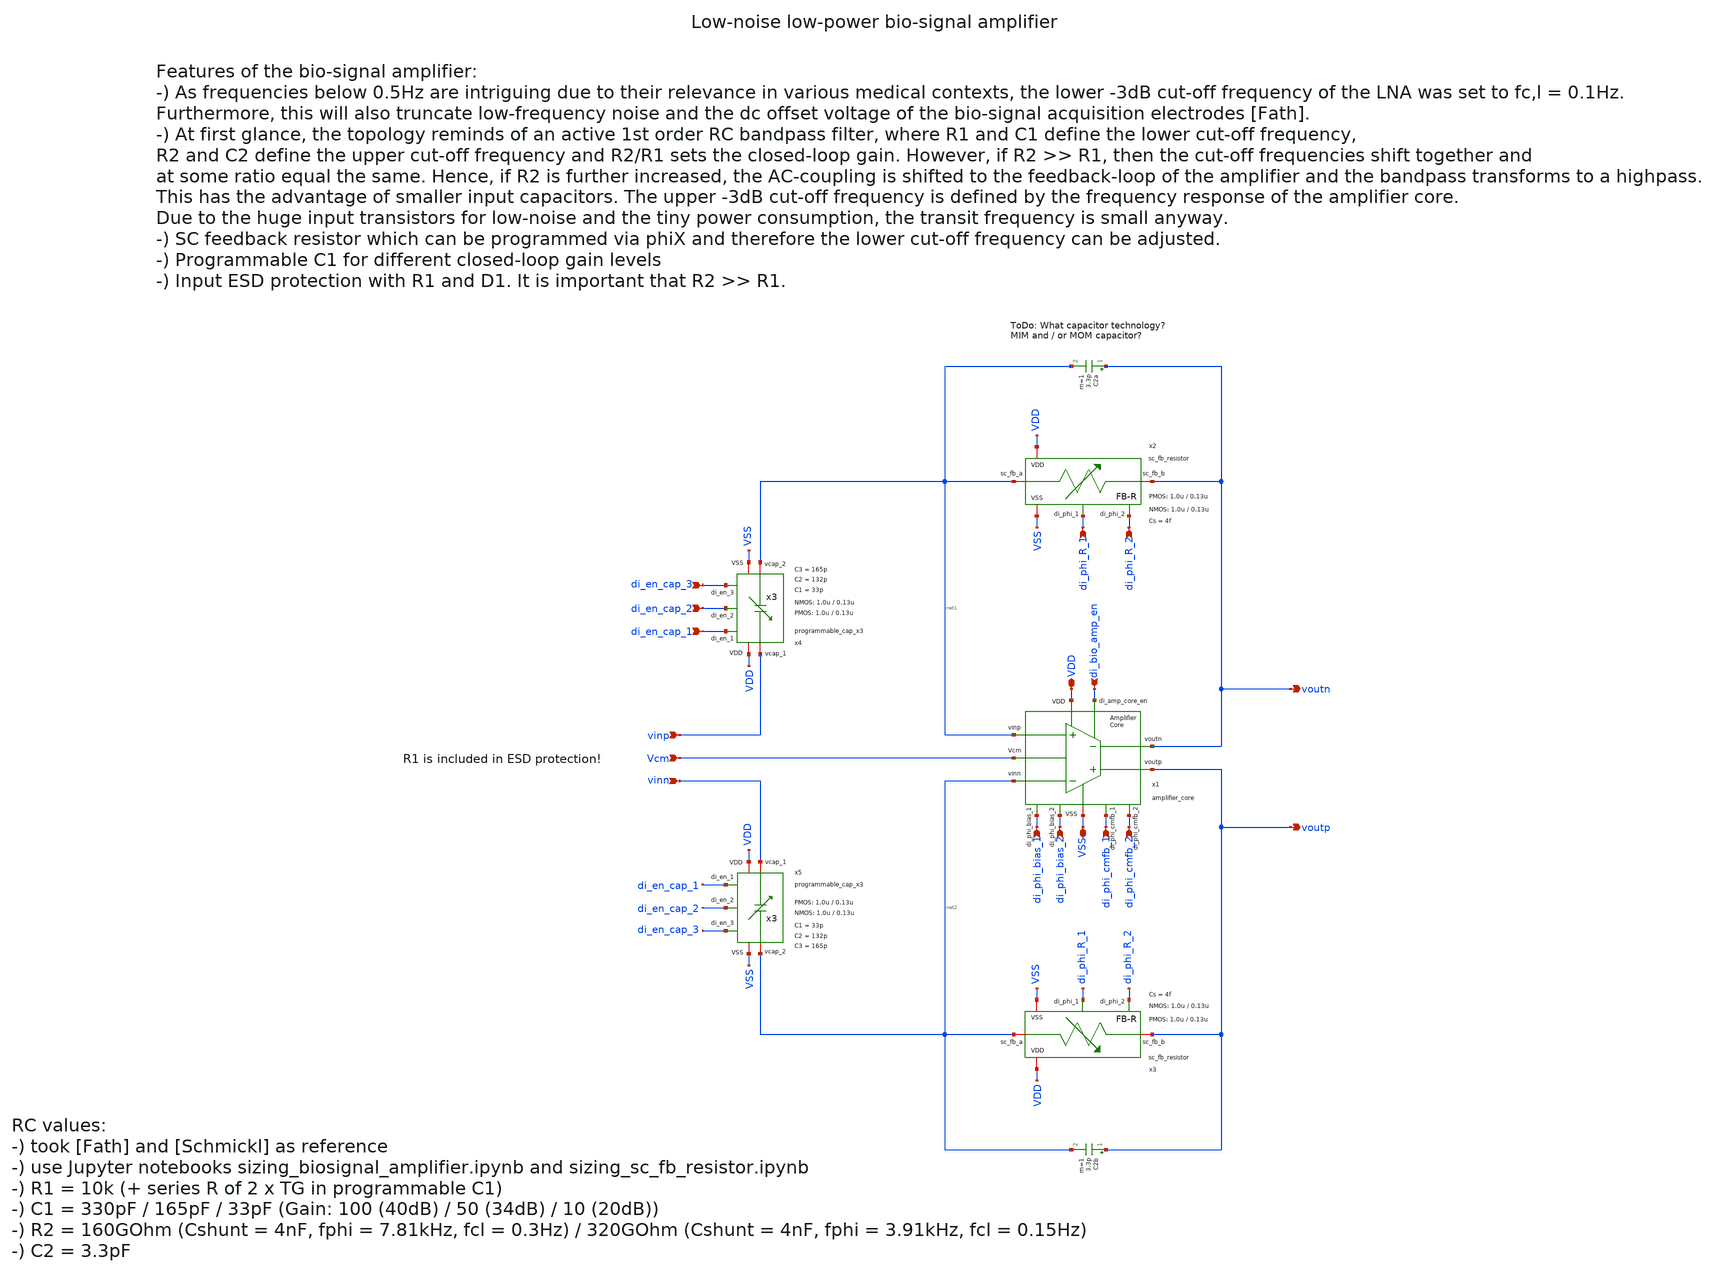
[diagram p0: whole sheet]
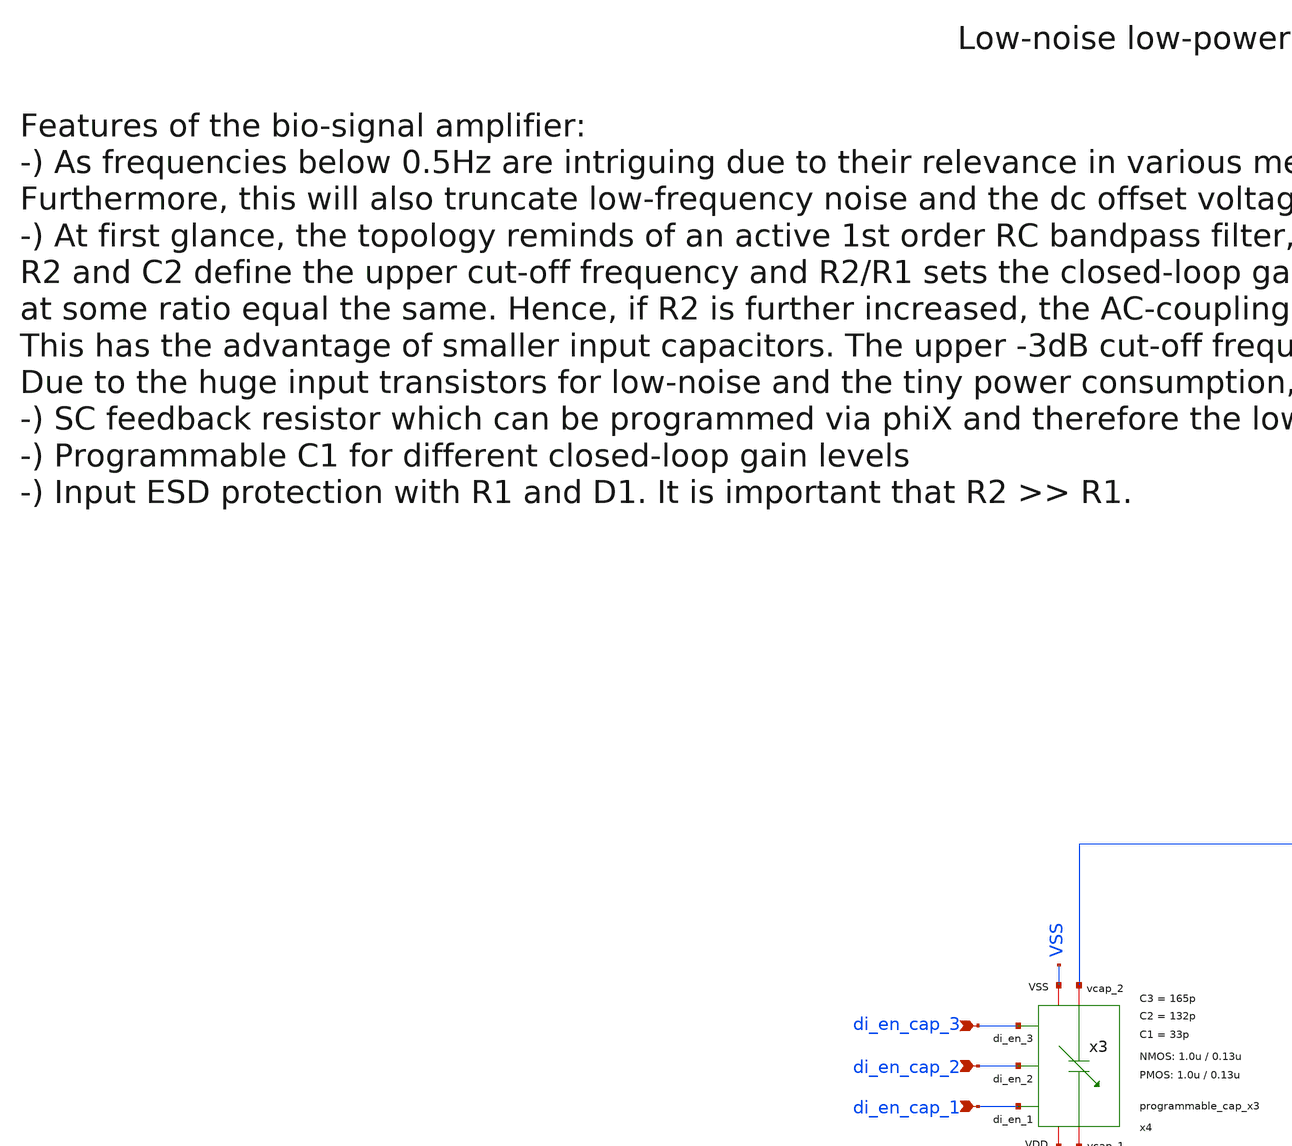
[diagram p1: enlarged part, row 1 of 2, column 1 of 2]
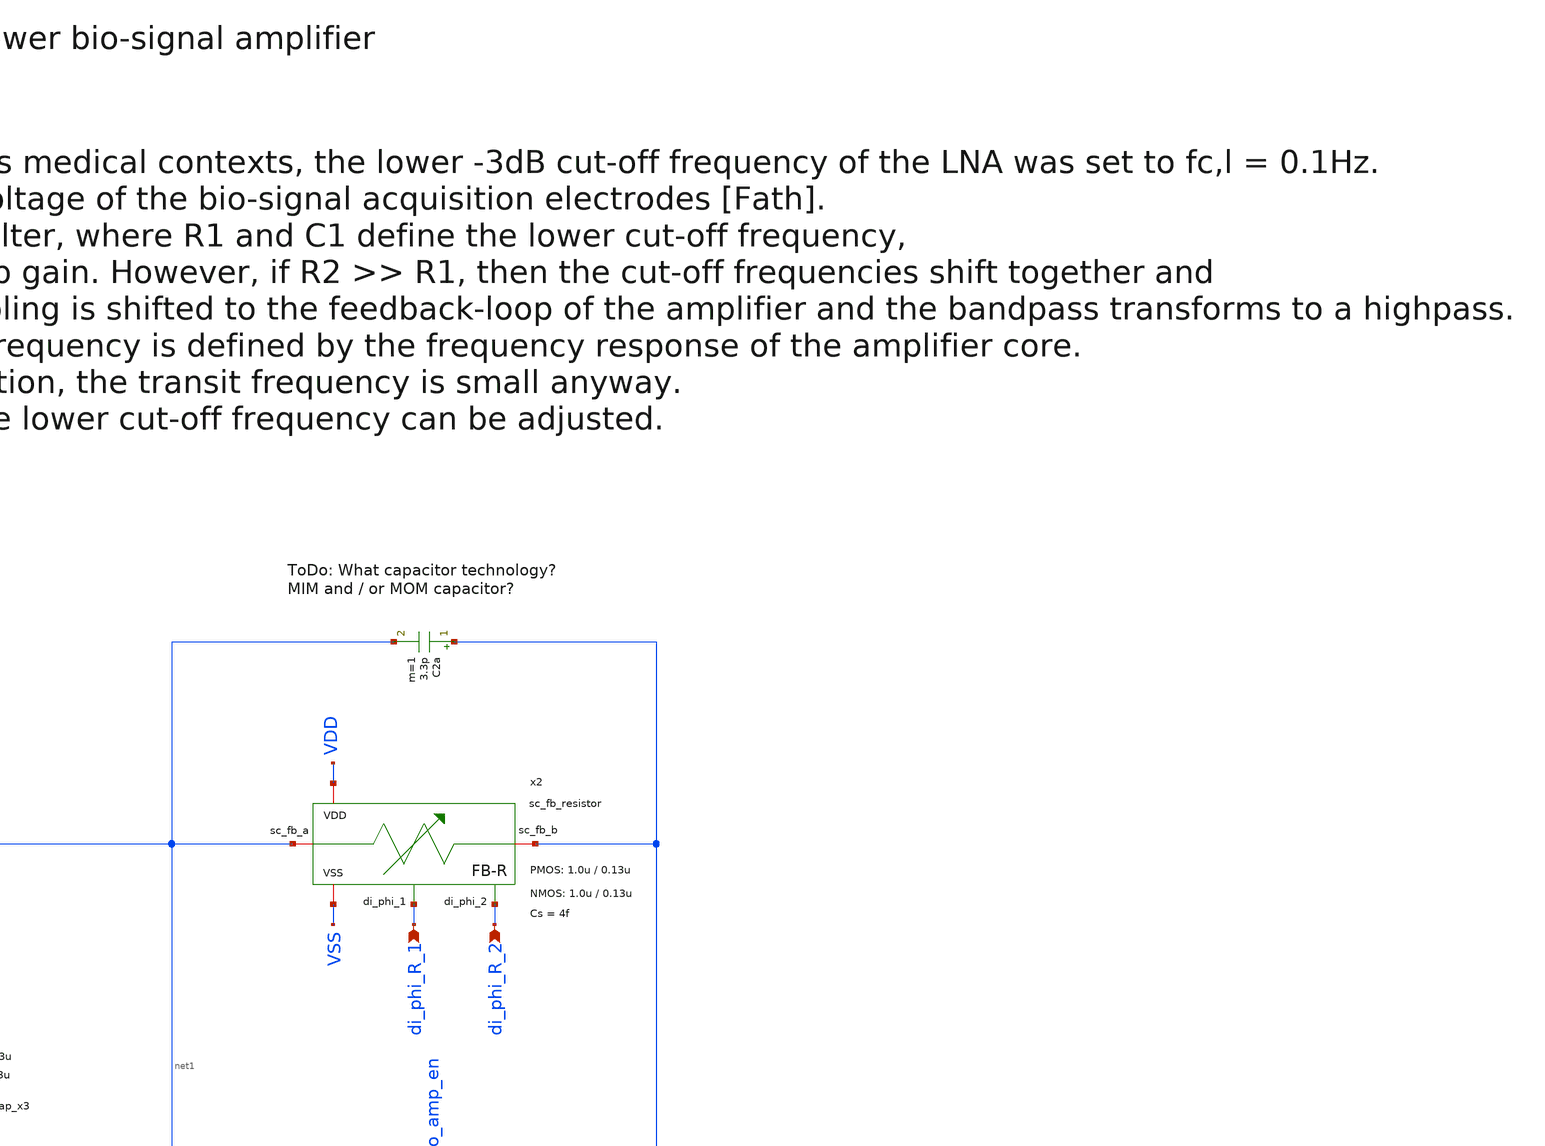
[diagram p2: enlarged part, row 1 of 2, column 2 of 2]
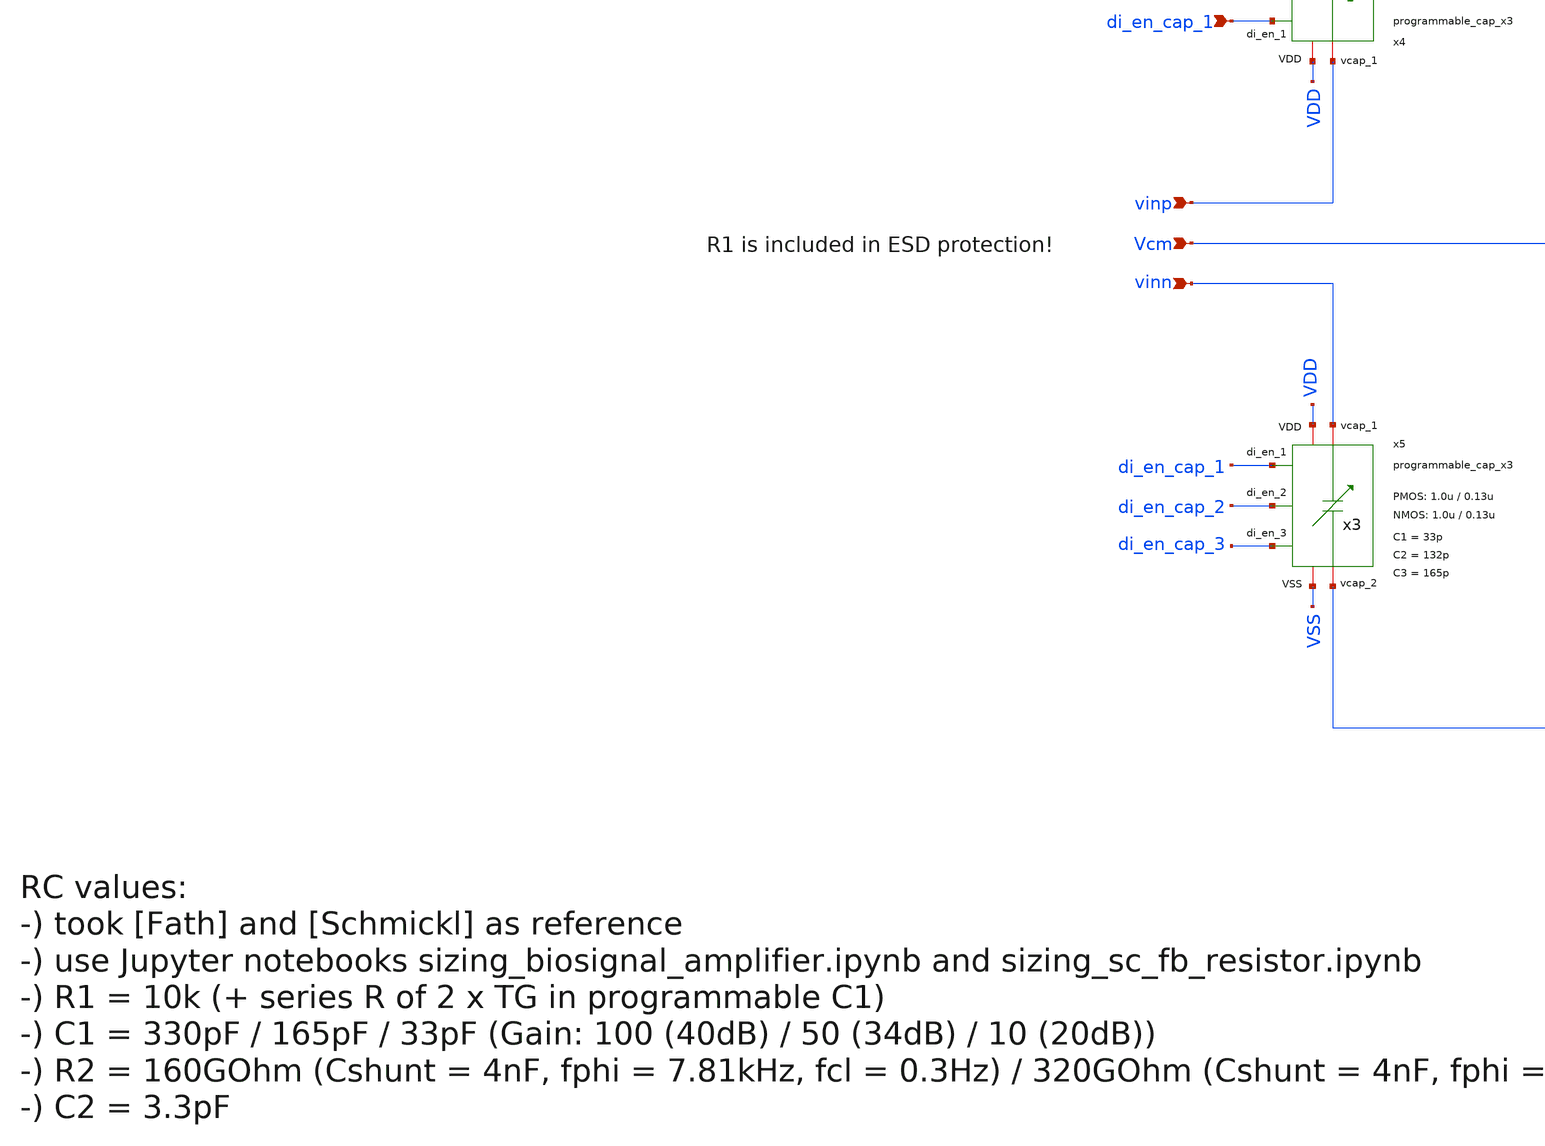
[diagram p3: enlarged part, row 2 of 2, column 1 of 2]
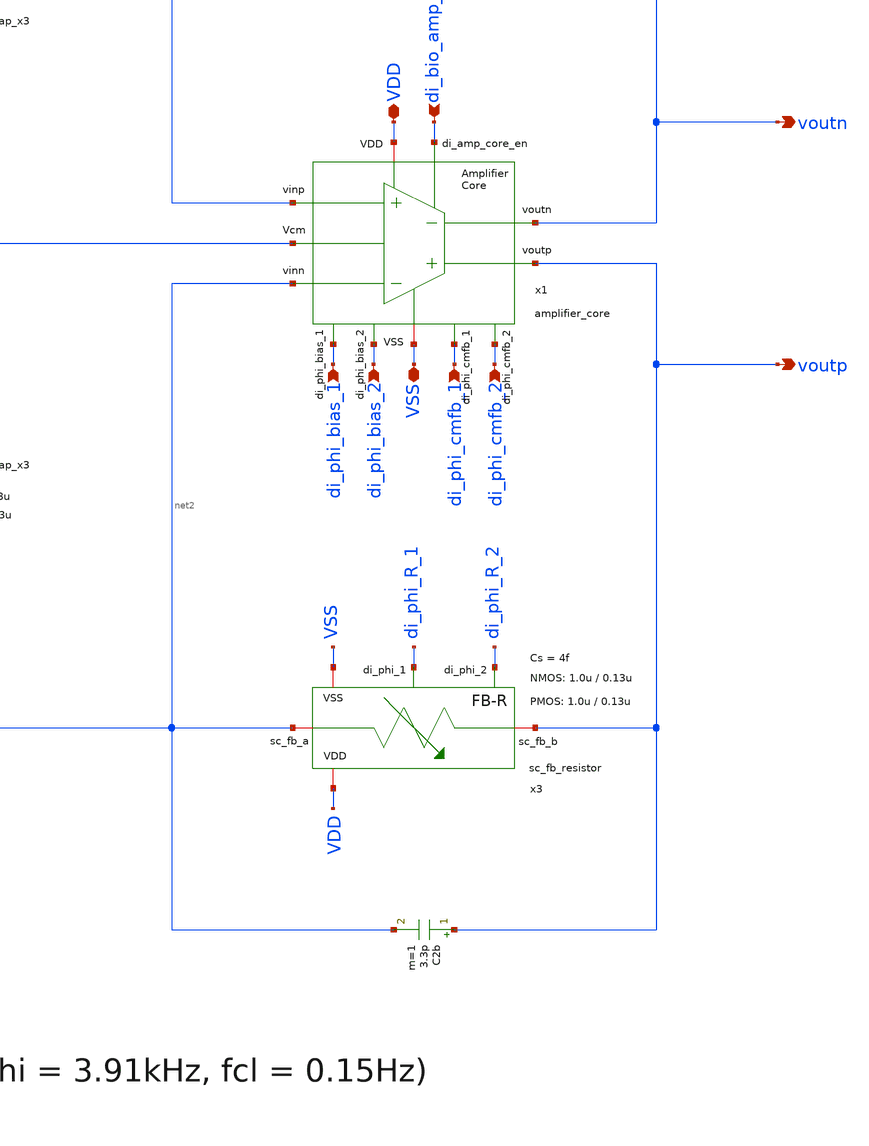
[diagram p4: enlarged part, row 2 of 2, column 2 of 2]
** sch_path: SG13G2_ATBS-ADC-main/xschem/bio_amplifier/bio_amplifier.sch
**.subckt bio_amplifier VDD VSS di_bio_amp_en vinp vinn Vcm voutp voutn di_phi_cmfb_1 di_phi_cmfb_2
*+ di_phi_R_1 di_phi_R_2 di_phi_bias_1 di_phi_bias_2 di_en_cap_1 di_en_cap_2 di_en_cap_3
*.iopin VDD
*.iopin VSS
*.ipin di_bio_amp_en
*.ipin vinp
*.ipin vinn
*.ipin Vcm
*.opin voutp
*.opin voutn
*.ipin di_phi_cmfb_1
*.ipin di_phi_cmfb_2
*.ipin di_phi_R_1
*.ipin di_phi_R_2
*.ipin di_phi_bias_1
*.ipin di_phi_bias_2
*.ipin di_en_cap_1
*.ipin di_en_cap_2
*.ipin di_en_cap_3
x2 net1 voutn di_phi_R_2 di_phi_R_1 VDD VSS sc_fb_resistor W_P_FB=1.0u L_P_FB=0.13u W_N_FB=1.0u
+ L_N_FB=0.13u Cs=4f
x3 net2 voutp di_phi_R_2 di_phi_R_1 VDD VSS sc_fb_resistor W_P_FB=1.0u L_P_FB=0.13u W_N_FB=1.0u
+ L_N_FB=0.13u Cs=4f
C2a voutn net1 3.3p m=1
C2b voutp net2 3.3p m=1
x4 VDD di_en_cap_1 VSS di_en_cap_2 vinp net1 di_en_cap_3 programmable_cap_x3 W_P_PC=1.0u
+ L_P_PC=0.13u W_N_PC=1.0u L_N_PC=0.13u C1=33p C2=132p C3=165p
x5 VDD di_en_cap_1 VSS di_en_cap_2 vinn net2 di_en_cap_3 programmable_cap_x3 W_P_PC=1.0u
+ L_P_PC=0.13u W_N_PC=1.0u L_N_PC=0.13u C1=33p C2=132p C3=165p
x1 di_phi_cmfb_1 di_phi_bias_2 di_phi_bias_1 di_phi_cmfb_2 voutp voutn di_bio_amp_en net2 net1 VDD
+ VSS Vcm amplifier_core
**.ends
.end
